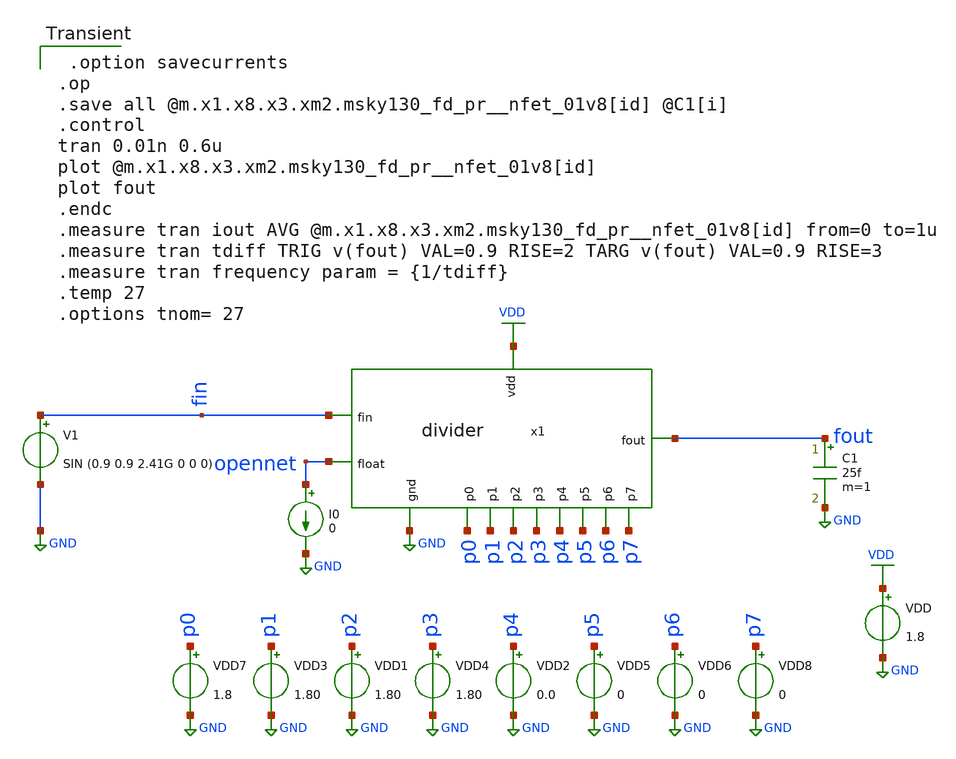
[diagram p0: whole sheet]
** sch_path: pll/dividers_lib/divider_tb/xschem/divider_tb.sch
**.subckt divider_tb
VDD VDD GND 1.8
VDD1 p2 GND 1.80
VDD2 p4 GND 0.0
VDD3 p1 GND 1.80
VDD4 p3 GND 1.80
VDD5 p5 GND 0
VDD6 p6 GND 0
VDD7 p0 GND 1.8
VDD8 p7 GND 0
x1 VDD fout GND p2 p7 p1 p6 p5 p4 p3 p0 fin opennet divider
V1 fin GND SIN (0.9 0.9 2.41G 0 0 0)
C1 fout GND 25f m=1
I0 opennet GND 0
**** begin user architecture code

** opencircuitdesign pdks install
.lib $::SKYWATER_MODELS/sky130.lib.spice tt



 .option savecurrents
.op
.save all @m.x1.x8.x3.xm2.msky130_fd_pr__nfet_01v8[id] @C1[i]
.control
tran 0.01n 0.6u
plot @m.x1.x8.x3.xm2.msky130_fd_pr__nfet_01v8[id]
plot fout
.endc
.measure tran iout AVG @m.x1.x8.x3.xm2.msky130_fd_pr__nfet_01v8[id] from=0 to=1u
.measure tran tdiff TRIG v(fout) VAL=0.9 RISE=2 TARG v(fout) VAL=0.9 RISE=3
.measure tran frequency param = {1/tdiff}
.temp 27
.options tnom= 27

**** end user architecture code
**.ends
.GLOBAL VDD
.GLOBAL GND
.end
